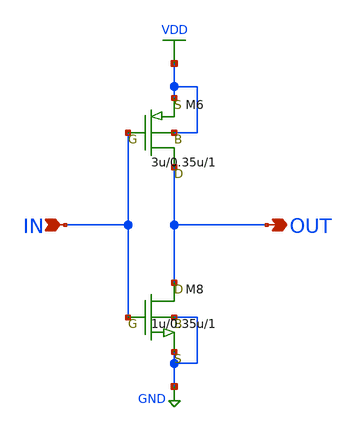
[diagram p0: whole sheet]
** sch_path: LR_hokari/LR_Work2/symbol/INVERTER.sch
**.subckt INVERTER OUT IN
*.opin OUT
*.ipin IN
M6 OUT IN VDD VDD pch w=3u l=0.35u as=0 ps=0 ad=0 pd=0 m=1
M8 OUT IN GND GND nch w=1u l=0.35u as=0 ps=0 ad=0 pd=0 m=1
**.ends
.GLOBAL VDD
.GLOBAL GND
.end
